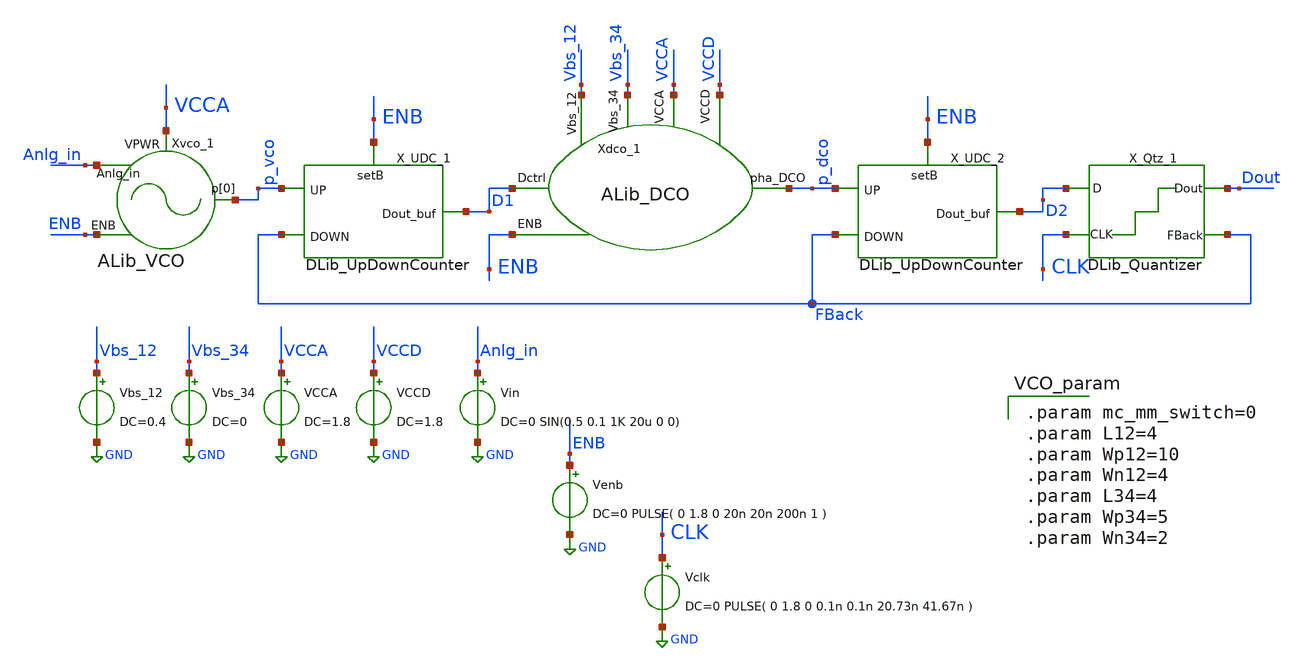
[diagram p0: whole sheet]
** sch_path: xschem/tb/VCO_ADC_tb.sch
**.subckt VCO_ADC_tb
Xvco_1 VCCA p_vco Anlg_in ENB ALib_VCO L12=L12 Wp12=Wp12 Wn12=Wn12 L34=L34 Wp34=Wp34 Wn34=Wn34
Xdco_1 D1 ENB Vbs_12 Vbs_34 VCCD VCCA p_dco ALib_DCO
X_UDC_1 p_vco FBack ENB GND GND VCCD VCCD D1 DLib_UpDownCounter
X_UDC_2 p_dco FBack ENB GND GND VCCD VCCD D2 DLib_UpDownCounter
X_Qtz_1 CLK D2 GND GND VCCD VCCD Dout FBack DLib_Quantizer
Vbs_34 Vbs_34 GND DC=0
VCCA VCCA GND DC=1.8
VCCD VCCD GND DC=1.8
Vin Anlg_in GND DC=0 SIN(0.5 0.1 1K 20u 0 0)
Venb ENB GND DC=0 PULSE( 0 1.8 0 20n 20n 200n 1 )
Vclk CLK GND DC=0 PULSE( 0 1.8 0 0.1n 0.1n 20.73n 41.67n )
Vbs_12 Vbs_12 GND DC=0.4
**** begin user architecture code


** Library on VNU server
*.lib /home/dkits/efabless/mpw-5/pdks/sky130A/libs.tech/ngspice/sky130.lib.spice tt
*.inc /home/dkits/efabless/mpw-5/pdks/sky130A/libs.ref/sky130_fd_sc_hd/spice/sky130_fd_sc_hd.spice
** Library on Home PC
.lib /home/dkit/efabless/pdks/sky130A/libs.tech/ngspice/sky130.lib.spice tt
.inc /home/dkit/efabless/pdks/sky130A/libs.ref/sky130_fd_sc_hd/spice/sky130_fd_sc_hd.spice




.control
   tran 0.2n 10u
   plot p_vco/2+6 D1/2+5 p_dco/2+4 Xdco_1.p_osc/2+4 CLK/2+3 D2/2+2 Dout/2+1 FBack/2+0.05
.endc






.param mc_mm_switch=0
.param L12=4
.param Wp12=10
.param Wn12=4
.param L34=4
.param Wp34=5
.param Wn34=2

**** end user architecture code
**.ends
.GLOBAL GND
.end
